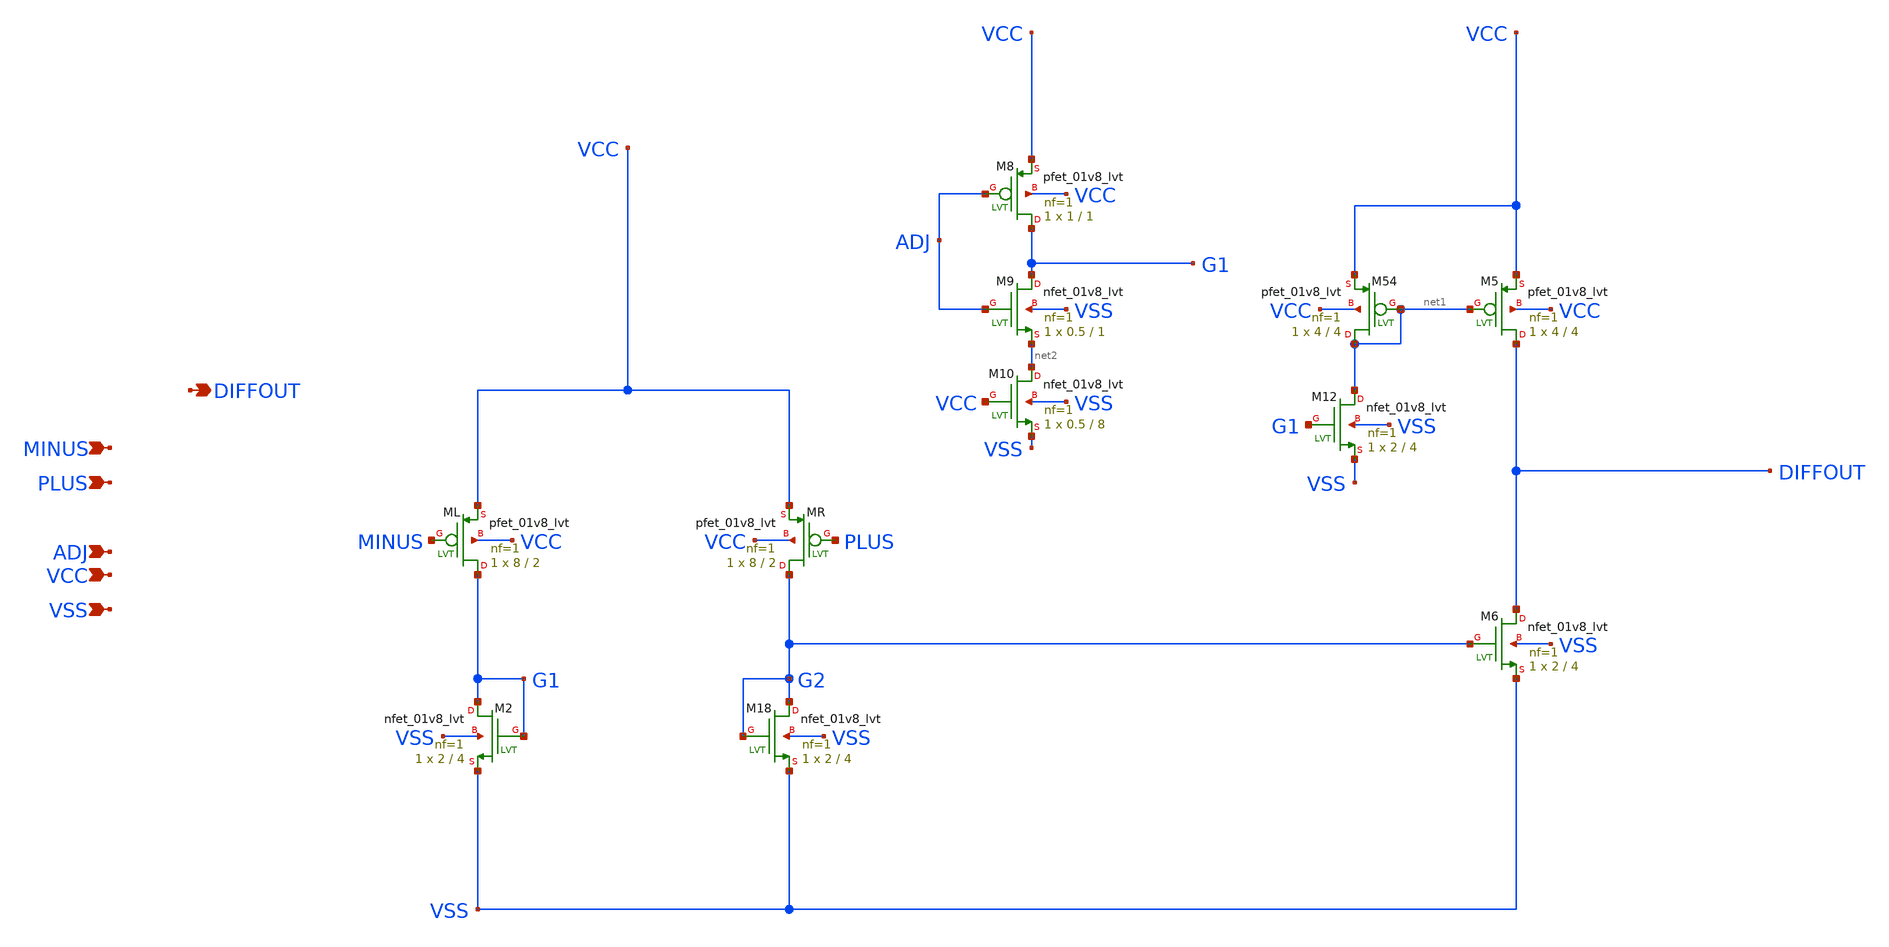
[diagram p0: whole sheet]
** sch_path: schematic/opamp.sch
**.subckt opamp PLUS MINUS VSS VCC DIFFOUT ADJ
*.ipin PLUS
*.ipin MINUS
*.ipin VSS
*.ipin VCC
*.opin DIFFOUT
*.ipin ADJ
XM18 G2 G2 VSS VSS sky130_fd_pr__nfet_01v8_lvt L=4 W=2 nf=1 ad='W * 0.29' as='W * 0.29' pd='2*(W + 0.29)'
+ ps='2*(W + 0.29)' nrd=0 nrs=0 sa=0 sb=0 sd=0 mult=1 m=1
XM2 G1 G1 VSS VSS sky130_fd_pr__nfet_01v8_lvt L=4 W=2 nf=1 ad='W * 0.29' as='W * 0.29' pd='2*(W + 0.29)'
+ ps='2*(W + 0.29)' nrd=0 nrs=0 sa=0 sb=0 sd=0 mult=1 m=1
XMR G2 PLUS VCC VCC sky130_fd_pr__pfet_01v8_lvt L=2 W=8 nf=1 ad='W * 0.29' as='W * 0.29' pd='2*(W + 0.29)'
+ ps='2*(W + 0.29)' nrd=0 nrs=0 sa=0 sb=0 sd=0 mult=1 m=1
XML G1 MINUS VCC VCC sky130_fd_pr__pfet_01v8_lvt L=2 W=8 nf=1 ad='W * 0.29' as='W * 0.29' pd='2*(W + 0.29)'
+ ps='2*(W + 0.29)' nrd=0 nrs=0 sa=0 sb=0 sd=0 mult=1 m=1
XM6 DIFFOUT G2 VSS VSS sky130_fd_pr__nfet_01v8_lvt L=4 W=2 nf=1 ad='W * 0.29' as='W * 0.29' pd='2*(W + 0.29)'
+ ps='2*(W + 0.29)' nrd=0 nrs=0 sa=0 sb=0 sd=0 mult=1 m=1
XM12 net1 G1 VSS VSS sky130_fd_pr__nfet_01v8_lvt L=4 W=2 nf=1 ad='W * 0.29' as='W * 0.29' pd='2*(W + 0.29)'
+ ps='2*(W + 0.29)' nrd=0 nrs=0 sa=0 sb=0 sd=0 mult=1 m=1
XM54 net1 net1 VCC VCC sky130_fd_pr__pfet_01v8_lvt L=4 W=4 nf=1 ad='W * 0.29' as='W * 0.29' pd='2*(W + 0.29)'
+ ps='2*(W + 0.29)' nrd=0 nrs=0 sa=0 sb=0 sd=0 mult=1 m=1
XM5 DIFFOUT net1 VCC VCC sky130_fd_pr__pfet_01v8_lvt L=4 W=4 nf=1 ad='W * 0.29' as='W * 0.29' pd='2*(W + 0.29)'
+ ps='2*(W + 0.29)' nrd=0 nrs=0 sa=0 sb=0 sd=0 mult=1 m=1
XM8 G1 ADJ VCC VCC sky130_fd_pr__pfet_01v8_lvt L=1 W=1 nf=1 ad='W * 0.29' as='W * 0.29' pd='W + 2 * 0.29'
+ ps='W + 2 * 0.29' nrd=0 nrs=0 sa=0 sb=0 sd=0 mult=1 m=1
XM9 G1 ADJ net2 VSS sky130_fd_pr__nfet_01v8_lvt L=1 W=0.5 nf=1 ad='W * 0.29' as='W * 0.29' pd='W + 2 * 0.29'
+ ps='W + 2 * 0.29' nrd=0 nrs=0 sa=0 sb=0 sd=0 mult=1 m=1
XM10 net2 VCC VSS VSS sky130_fd_pr__nfet_01v8_lvt L=8 W=0.5 nf=1 ad='W * 0.29' as='W * 0.29' pd='2*(W + 0.29)'
+ ps='2*(W + 0.29)' nrd=0 nrs=0 sa=0 sb=0 sd=0 mult=1 m=1
**.ends
.end
